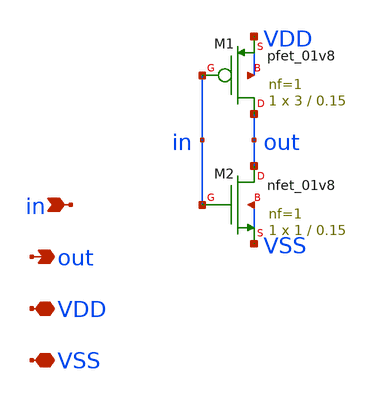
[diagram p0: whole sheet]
** sch_path: xschem/inverter_2.sch
**.subckt inverter_2 VDD in out VSS
*.iopin VDD
*.ipin in
*.opin out
*.iopin VSS
XM1 out in VDD VDD sky130_fd_pr__pfet_01v8 L=0.15 W=3 nf=1 ad='int((nf+1)/2) * W/nf * 0.29' as='int((nf+2)/2) * W/nf * 0.29'
+ pd='2*int((nf+1)/2) * (W/nf + 0.29)' ps='2*int((nf+2)/2) * (W/nf + 0.29)' nrd='0.29 / W' nrs='0.29 / W'
+ sa=0 sb=0 sd=0 mult=1 m=1
XM2 out in VSS VSS sky130_fd_pr__nfet_01v8 L=0.15 W=1 nf=1 ad='int((nf+1)/2) * W/nf * 0.29' as='int((nf+2)/2) * W/nf * 0.29'
+ pd='2*int((nf+1)/2) * (W/nf + 0.29)' ps='2*int((nf+2)/2) * (W/nf + 0.29)' nrd='0.29 / W' nrs='0.29 / W'
+ sa=0 sb=0 sd=0 mult=1 m=1
**.ends
.end
